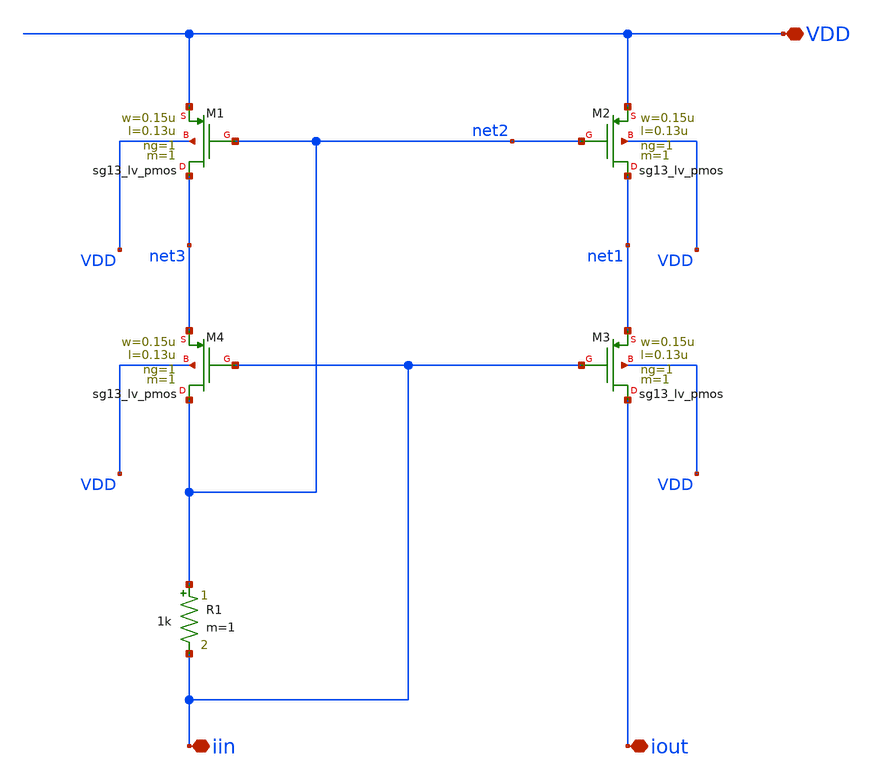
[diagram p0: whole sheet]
** sch_path: analog-db/templates/current_mirror/pmos_current_source/selfbiased_high_swing_cascode_current_mirror.sch
* Copyright 2026 MacAnalog Research Group
**.subckt selfbiased_high_swing_cascode_current_mirror VDD iout iin
*.iopin VDD
*.iopin iout
*.iopin iin
XM1 net3 net2 VDD VDD sg13_lv_pmos w=0.15u l=0.13u ng=1 m=1 mm_ok=1
XM2 net1 net2 VDD VDD sg13_lv_pmos w=0.15u l=0.13u ng=1 m=1 mm_ok=1
XM3 iout iin net1 VDD sg13_lv_pmos w=0.15u l=0.13u ng=1 m=1 mm_ok=1
XM4 net2 iin net3 VDD sg13_lv_pmos w=0.15u l=0.13u ng=1 m=1 mm_ok=1
R1 net2 iin 1k m=1
**.ends
.end
